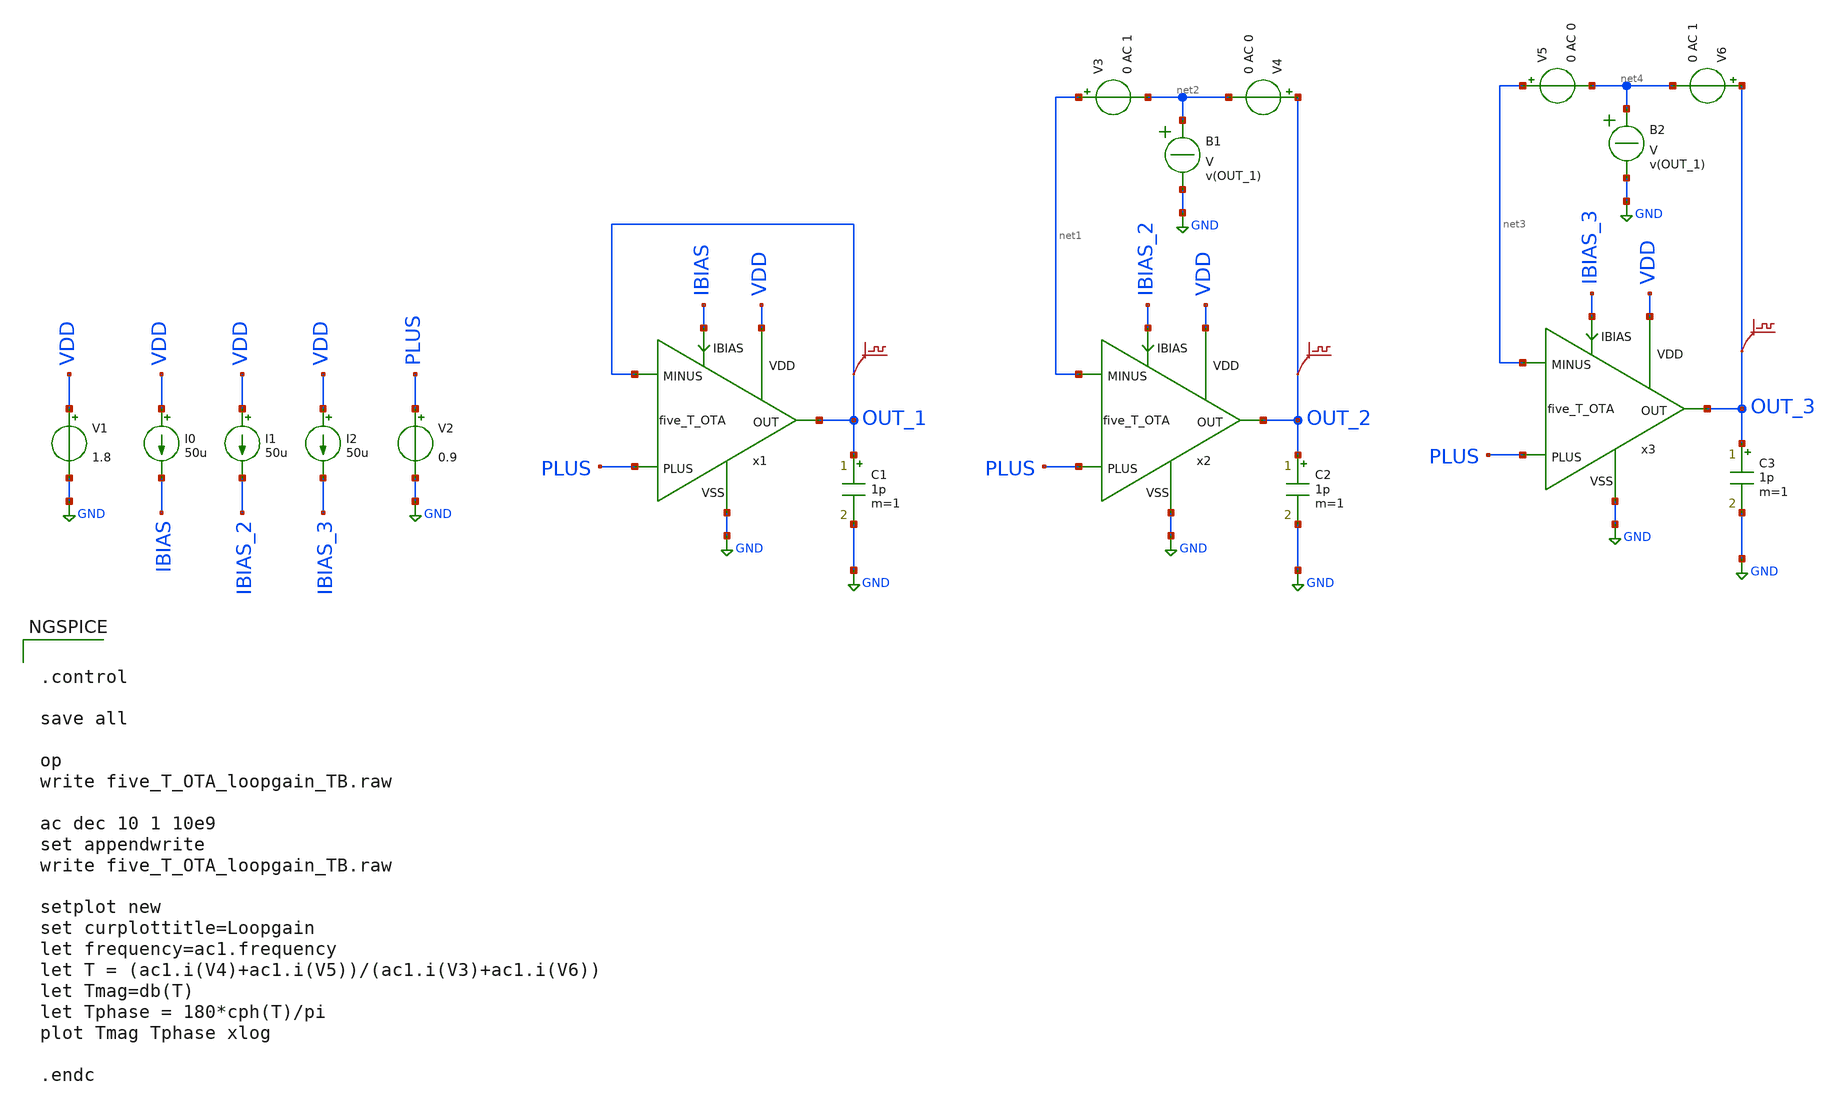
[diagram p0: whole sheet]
** sch_path: examples/xschem/five_T_OTA_loopgain_TB.sch
**.subckt five_T_OTA_loopgain_TB
x1 OUT_1 OUT_1 PLUS IBIAS GND VDD five_T_OTA
V1 VDD GND 1.8
I0 VDD IBIAS 50u
V2 PLUS GND 0.9
C1 OUT_1 GND 1p m=1
x2 OUT_2 net1 PLUS IBIAS_2 GND VDD five_T_OTA
C2 OUT_2 GND 1p m=1
V3 net1 net2 0 AC 1
V4 OUT_2 net2 0 AC 0
B1 net2 GND V = v(OUT_1)
x3 OUT_3 net3 PLUS IBIAS_3 GND VDD five_T_OTA
C3 OUT_3 GND 1p m=1
V5 net3 net4 0 AC 0
V6 OUT_3 net4 0 AC 1
B2 net4 GND V = v(OUT_1)
.save v(out_1)
.save v(out_2)
.save v(out_3)
I1 VDD IBIAS_2 50u
I2 VDD IBIAS_3 50u
**** begin user architecture code


.control

save all

op
write five_T_OTA_loopgain_TB.raw

ac dec 10 1 10e9
set appendwrite
write five_T_OTA_loopgain_TB.raw

setplot new
set curplottitle=Loopgain
let frequency=ac1.frequency
let T = (ac1.i(V4)+ac1.i(V5))/(ac1.i(V3)+ac1.i(V6))
let Tmag=db(T)
let Tphase = 180*cph(T)/pi
plot Tmag Tphase xlog

.endc



** opencircuitdesign pdks install
.lib $::SKYWATER_MODELS/sky130.lib.spice tt


**** end user architecture code
**.ends

* expanding   symbol:  five_T_OTA.sym # of pins=6
** sym_path: examples/xschem/five_T_OTA.sym
** sch_path: examples/xschem/five_T_OTA.sch
.subckt five_T_OTA OUT MINUS PLUS IBIAS VSS VDD
*.iopin VDD
*.iopin VSS
*.iopin MINUS
*.iopin PLUS
*.iopin OUT
*.iopin IBIAS
XM2 IBIAS IBIAS VSS VSS sky130_fd_pr__nfet_01v8 L=0.3 W=3 nf=1 ad='int((nf+1)/2) * W/nf * 0.29' as='int((nf+2)/2) * W/nf * 0.29'
+ pd='2*int((nf+1)/2) * (W/nf + 0.29)' ps='2*int((nf+2)/2) * (W/nf + 0.29)' nrd='0.29 / W' nrs='0.29 / W'
+ sa=0 sb=0 sd=0 mult=1 m=1
XM1 net1 IBIAS VSS VSS sky130_fd_pr__nfet_01v8 L=0.3 W=3 nf=1 ad='int((nf+1)/2) * W/nf * 0.29' as='int((nf+2)/2) * W/nf * 0.29'
+ pd='2*int((nf+1)/2) * (W/nf + 0.29)' ps='2*int((nf+2)/2) * (W/nf + 0.29)' nrd='0.29 / W' nrs='0.29 / W'
+ sa=0 sb=0 sd=0 mult=4 m=4
.save v(ibias)
.save v(out)
.save v(net2)
.save v(net1)
XM4 net2 PLUS net1 VSS sky130_fd_pr__nfet_01v8_lvt L=0.3 W=4 nf=1 ad='int((nf+1)/2) * W/nf * 0.29' as='int((nf+2)/2) * W/nf * 0.29'
+ pd='2*int((nf+1)/2) * (W/nf + 0.29)' ps='2*int((nf+2)/2) * (W/nf + 0.29)' nrd='0.29 / W' nrs='0.29 / W'
+ sa=0 sb=0 sd=0 mult=4 m=4
XM5 OUT MINUS net1 VSS sky130_fd_pr__nfet_01v8_lvt L=0.3 W=4 nf=1 ad='int((nf+1)/2) * W/nf * 0.29' as='int((nf+2)/2) * W/nf * 0.29'
+ pd='2*int((nf+1)/2) * (W/nf + 0.29)' ps='2*int((nf+2)/2) * (W/nf + 0.29)' nrd='0.29 / W' nrs='0.29 / W'
+ sa=0 sb=0 sd=0 mult=4 m=4
XM3 net2 net2 VDD VDD sky130_fd_pr__pfet_01v8_lvt L=0.7 W=2.3 nf=1 ad='int((nf+1)/2) * W/nf * 0.29' as='int((nf+2)/2) * W/nf * 0.29'
+ pd='2*int((nf+1)/2) * (W/nf + 0.29)' ps='2*int((nf+2)/2) * (W/nf + 0.29)' nrd='0.29 / W' nrs='0.29 / W'
+ sa=0 sb=0 sd=0 mult=4 m=4
XM6 OUT net2 VDD VDD sky130_fd_pr__pfet_01v8_lvt L=0.7 W=2.3 nf=1 ad='int((nf+1)/2) * W/nf * 0.29' as='int((nf+2)/2) * W/nf * 0.29'
+ pd='2*int((nf+1)/2) * (W/nf + 0.29)' ps='2*int((nf+2)/2) * (W/nf + 0.29)' nrd='0.29 / W' nrs='0.29 / W'
+ sa=0 sb=0 sd=0 mult=4 m=4
.ends

.GLOBAL GND
.end
